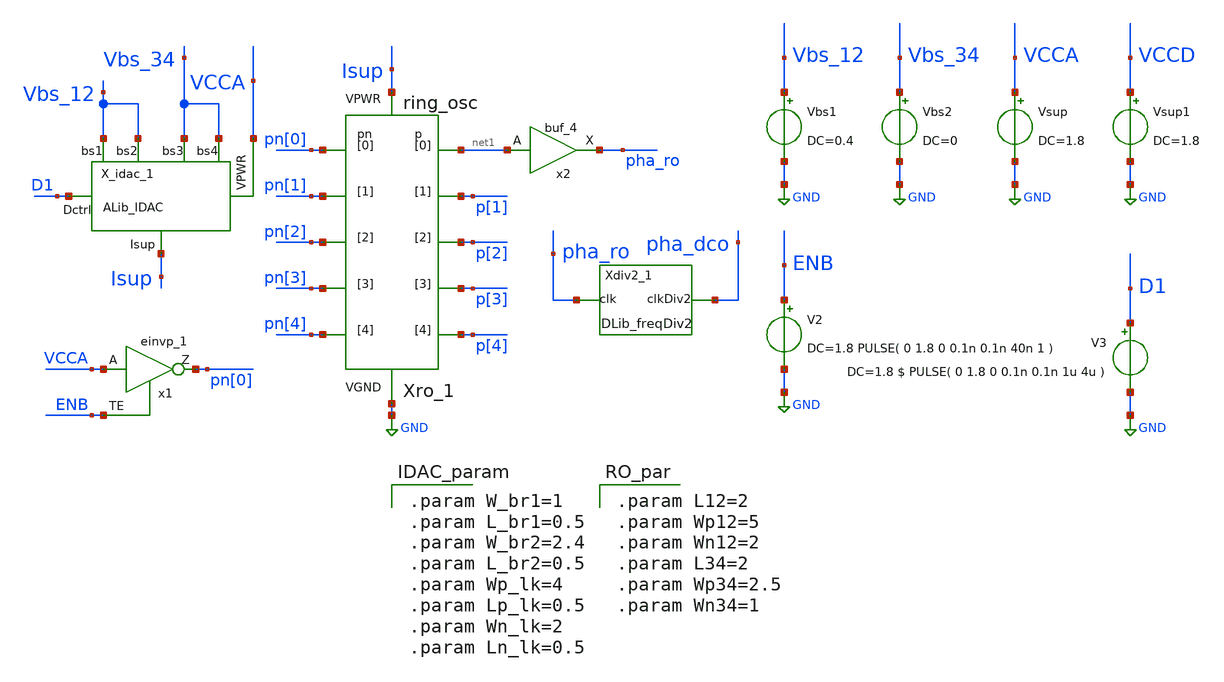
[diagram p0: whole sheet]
** sch_path: xschem/tb/IDAC_tb.sch
**.subckt IDAC_tb
Vsup VCCA GND DC=1.8
Vbs1 Vbs_12 GND DC=0.4
x1 VCCA ENB VGND VNB VPB VPWR pn[0] sky130_fd_sc_hd__einvp_1
V2 ENB GND DC=1.8 PULSE( 0 1.8 0 0.1n 0.1n 40n 1 )
V3 D1 GND DC=1.8 $ PULSE( 0 1.8 0 0.1n 0.1n 1u 4u )
Xro_1 GND Isup net1 p[1] p[2] p[3] p[4] pn[0] pn[1] pn[2] pn[3] pn[4] ring_osc L12="L12" Wp12="Wp12"
+ Wn12="Wn12" L34="L34" Wp34="Wp34" Wn34="Wn34"
X_idac_1 D1 Vbs_12 Vbs_12 Vbs_34 Vbs_34 VCCA Isup ALib_IDAC W_br1="W_br1" L_br1="L_br1"
+ W_br2="W_br2" L_br2="L_br2" Wp_lk="Wp_lk" Lp_lk="Lp_lk" Wn_lk="Wn_lk" Ln_lk="Wn_lk"
Vbs2 Vbs_34 GND DC=0
x2 net1 GND GND VCCD VCCD pha_ro sky130_fd_sc_hd__buf_4
Vsup1 VCCD GND DC=1.8
Xdiv2_1 pha_ro GND GND VCCD VCCD pha_dco DLib_freqDiv2
**** begin user architecture code


** Library on VNU server
.lib /home/dkits/efabless/mpw-5/pdks/sky130A/libs.tech/ngspice/sky130.lib.spice tt
.inc /home/dkits/efabless/mpw-5/pdks/sky130A/libs.ref/sky130_fd_sc_hd/spice/sky130_fd_sc_hd.spice
** Library on Home PC
*.lib /home/dkit/efabless/pdks/sky130A/libs.tech/ngspice/sky130.lib.spice tt
*.inc /home/dkit/efabless/pdks/sky130A/libs.ref/sky130_fd_sc_hd/spice/sky130_fd_sc_hd.spice




.control
set nobreak
set num_threads=8
set test_mode = 0
* mode = 0: operation testing    1:  frequency extraction    2:  power consumption
if ($test_mode = 0)
    TRAN 1n 12u
    plot pha_dco
    MEAS TRAN prd TRIG pha_dco VAL=0.8 RISE=10 TARG pha_dco VAL=0.8 RISE=20
    let freq = 10/prd
    echo "frequency: "
    print freq
end
if ($test_mode = 1)
    let Vlow = 0
    let Vlimit = 1.01     $ set upper bound for sweeping
    let Vsweep = 0.2      $ set step size for sweeping
    let NoPoints=(Vlimit-Vlow)/Vsweep+2    $ set number of points for sweeping
    let freq =unitvec(NoPoints)
    let Vin  =unitvec(NoPoints)
    let Vin[0]=Vlow
    let ix=0
    while Vin[ix] < Vlimit
        alter Vground DC=Vin[ix]
        TRAN 0.4n 12u
        MEAS TRAN prd TRIG pha_dco VAL=0.8 RISE=10 TARG pha_dco VAL=0.8 RISE =20
        let freq[ix] = 10/prd
        let ix = ix+1
        Let Vin[ix] = Vin[ix-1]+Vsweep
    end
   print Vin freq
end
if ($test_mode = 2)
    save vdd @Vsup[i] pha_dco
    TRAN 0.1n 5u
    MEAS TRAN I_vco AVG @Vsup[i] FROM=3u TO=4u
    MEAS TRAN V_vco AVG vdd FROM=3u TO=4u
    let Power=I_vco*V_vco
    print Power
end
.endc



.param W_br1=1
.param L_br1=0.5
.param W_br2=2.4
.param L_br2=0.5
.param Wp_lk=4
.param Lp_lk=0.5
.param Wn_lk=2
.param Ln_lk=0.5


.param L12=2
.param Wp12=5
.param Wn12=2
.param L34=2
.param Wp34=2.5
.param Wn34=1

**** end user architecture code
**.ends
.GLOBAL GND
.end
